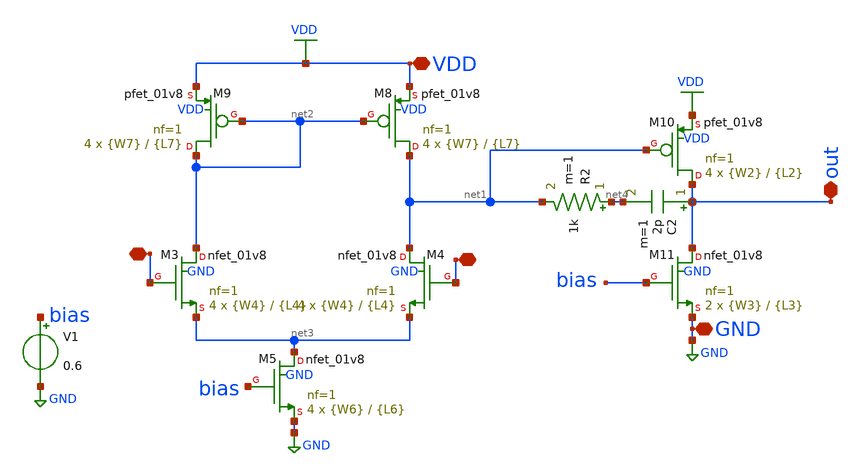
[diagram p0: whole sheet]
** sch_path: xschem/op5.2.sch
**.subckt op5.2 GND - + out VDD
*.iopin GND
*.iopin -
*.iopin +
*.iopin out
*.iopin VDD
C2 out net4 2p m=1
R2 net4 net1 1k m=1
XM3 net2 - net3 GND sky130_fd_pr__nfet_01v8 L={L4} W={W4} nf=1 ad='int((nf+1)/2) * W/nf * 0.29' as='int((nf+2)/2) * W/nf * 0.29'
+ pd='2*int((nf+1)/2) * (W/nf + 0.29)' ps='2*int((nf+2)/2) * (W/nf + 0.29)' nrd='0.29 / W' nrs='0.29 / W'
+ sa=0 sb=0 sd=0 mult=4 m=4
XM4 net1 + net3 GND sky130_fd_pr__nfet_01v8 L={L4} W={W4} nf=1 ad='int((nf+1)/2) * W/nf * 0.29' as='int((nf+2)/2) * W/nf * 0.29'
+ pd='2*int((nf+1)/2) * (W/nf + 0.29)' ps='2*int((nf+2)/2) * (W/nf + 0.29)' nrd='0.29 / W' nrs='0.29 / W'
+ sa=0 sb=0 sd=0 mult=4 m=4
XM8 net1 net2 VDD VDD sky130_fd_pr__pfet_01v8 L={L7} W={W7} nf=1 ad='int((nf+1)/2) * W/nf * 0.29' as='int((nf+2)/2) * W/nf * 0.29'
+ pd='2*int((nf+1)/2) * (W/nf + 0.29)' ps='2*int((nf+2)/2) * (W/nf + 0.29)' nrd='0.29 / W' nrs='0.29 / W'
+ sa=0 sb=0 sd=0 mult=4 m=4
XM9 net2 net2 VDD VDD sky130_fd_pr__pfet_01v8 L={L7} W={W7} nf=1 ad='int((nf+1)/2) * W/nf * 0.29' as='int((nf+2)/2) * W/nf * 0.29'
+ pd='2*int((nf+1)/2) * (W/nf + 0.29)' ps='2*int((nf+2)/2) * (W/nf + 0.29)' nrd='0.29 / W' nrs='0.29 / W'
+ sa=0 sb=0 sd=0 mult=4 m=4
XM5 net3 bias GND GND sky130_fd_pr__nfet_01v8 L={L6} W={W6} nf=1 ad='int((nf+1)/2) * W/nf * 0.29' as='int((nf+2)/2) * W/nf * 0.29'
+ pd='2*int((nf+1)/2) * (W/nf + 0.29)' ps='2*int((nf+2)/2) * (W/nf + 0.29)' nrd='0.29 / W' nrs='0.29 / W'
+ sa=0 sb=0 sd=0 mult=4 m=4
XM10 out net1 VDD VDD sky130_fd_pr__pfet_01v8 L={L2} W={W2} nf=1 ad='int((nf+1)/2) * W/nf * 0.29' as='int((nf+2)/2) * W/nf * 0.29'
+ pd='2*int((nf+1)/2) * (W/nf + 0.29)' ps='2*int((nf+2)/2) * (W/nf + 0.29)' nrd='0.29 / W' nrs='0.29 / W'
+ sa=0 sb=0 sd=0 mult=4 m=4
XM11 out bias GND GND sky130_fd_pr__nfet_01v8 L={L3} W={W3} nf=1 ad='int((nf+1)/2) * W/nf * 0.29' as='int((nf+2)/2) * W/nf * 0.29'
+ pd='2*int((nf+1)/2) * (W/nf + 0.29)' ps='2*int((nf+2)/2) * (W/nf + 0.29)' nrd='0.29 / W' nrs='0.29 / W'
+ sa=0 sb=0 sd=0 mult=2 m=2
V1 bias GND 0.6
**** begin user architecture code


**************
*PMOS cms
.param L1=2.7
.param W1=1.25

**************
*NMOS cms
.param L5=2
.param W5=3.5

**************
*PMOS current differential
.param L7=5
.param W7=1

**************
*differential Pair
.param L4=5
.param W4=1

**************
*NMOS current control
.param L6=5
.param W6=0.8

**************
*Second Stage
.param L2=10
.param W2=1

**************
*NMOS current second stage
.param L3=10
.param W3=1


**** end user architecture code
**.ends
.GLOBAL VDD
.GLOBAL GND
.end
